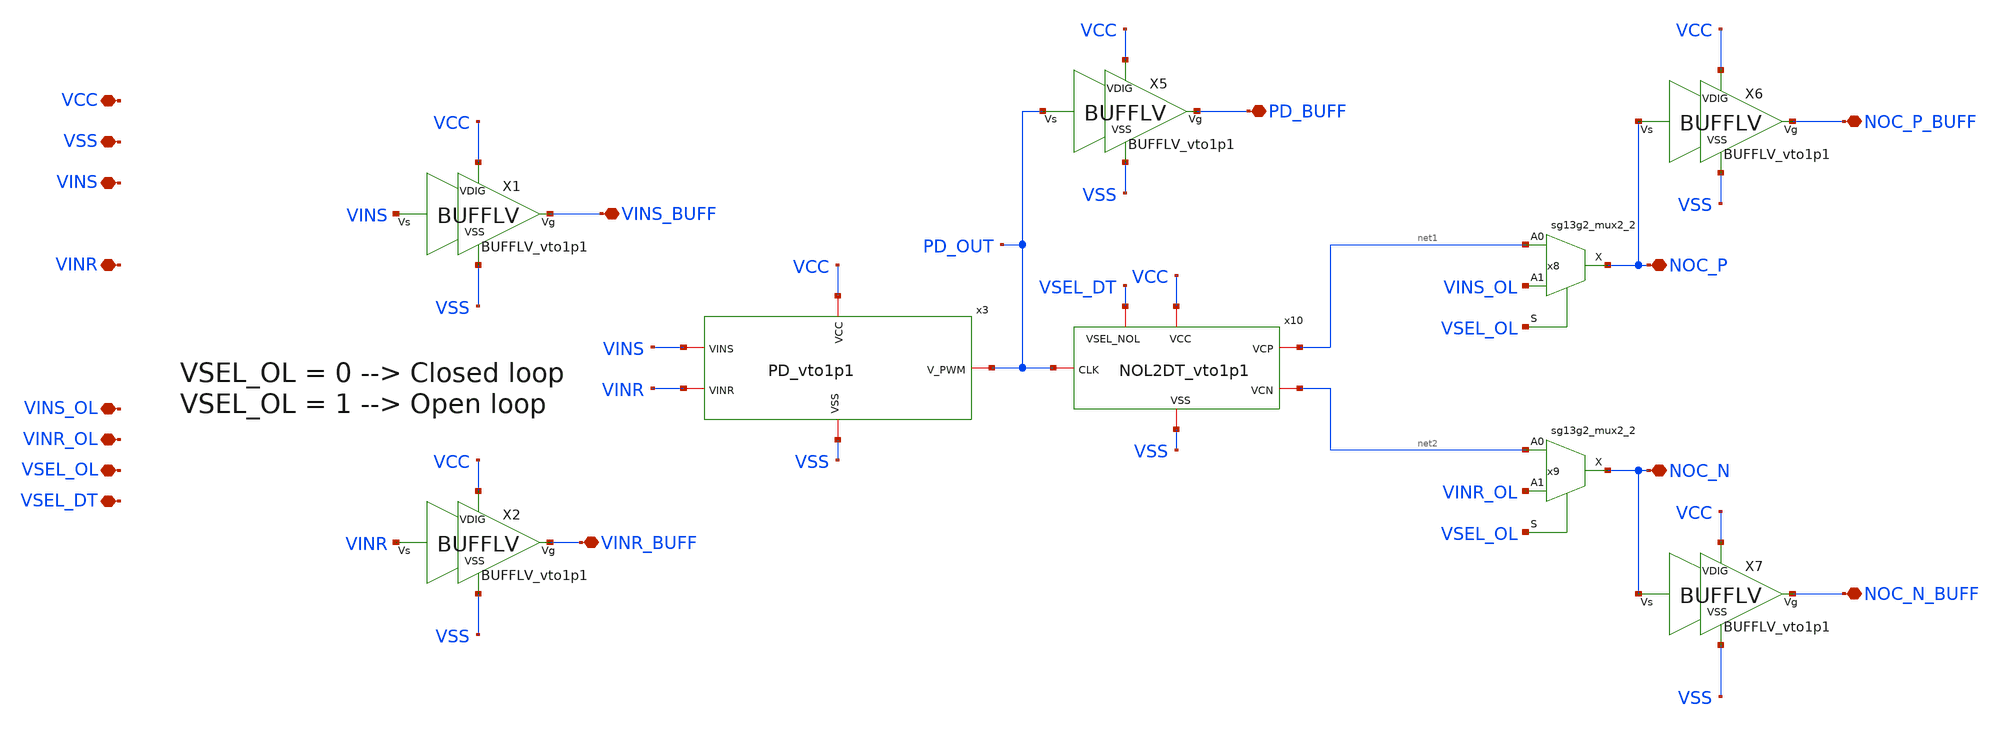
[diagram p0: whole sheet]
** sch_path: xschem/Digital_Block/DB.sch
* IHP-GmbH/IHP-Open-PDK/ihp-sg13g2/libs.tech/xschem/sg13g2_stdcells/sg13g2_buf_1.sch:
* Copyright 2023 IHP PDK Authors
* Licensed under the Apache License, Version 2.0 (the "License");
**.subckt DB VCC VSS VINS VINR NOC_P NOC_N VINS_BUFF VINR_BUFF PD_BUFF NOC_P_BUFF NOC_N_BUFF VINS_OL
*+ VINR_OL VSEL_OL VSEL_DT
*.iopin VCC
*.iopin VSS
*.iopin VINS
*.iopin VINR
*.iopin NOC_P
*.iopin NOC_N
*.iopin VINS_BUFF
*.iopin VINR_BUFF
*.iopin PD_BUFF
*.iopin NOC_P_BUFF
*.iopin NOC_N_BUFF
*.iopin VINS_OL
*.iopin VINR_OL
*.iopin VSEL_OL
*.iopin VSEL_DT
x3 VCC VSS VINS PD_OUT VINR PD_vto1p1
X1 VINS VINS_BUFF VCC VSS BUFFLV_vto1p1
X2 VINR VINR_BUFF VCC VSS BUFFLV_vto1p1
X5 PD_OUT PD_BUFF VCC VSS BUFFLV_vto1p1
X6 NOC_P NOC_P_BUFF VCC VSS BUFFLV_vto1p1
X7 NOC_N NOC_N_BUFF VCC VSS BUFFLV_vto1p1
x8 NOC_P net1 VINS_OL VSEL_OL VCC VSS sg13g2_mux2_2
x9 NOC_N net2 VINR_OL VSEL_OL VCC VSS sg13g2_mux2_2
x10 VCC VSS net1 PD_OUT net2 VSEL_DT NOL2DT_vto1p1
**.ends

* expanding   symbol:  xschem/PD/PD_vto1p1.sym # of pins=5
** sym_path: xschem/PD/PD_vto1p1.sym
** sch_path: xschem/PD/PD_vto1p1.sch
.subckt PD_vto1p1 VCC VSS VINS V_PWM VINR
*.iopin V_PWM
*.iopin VCC
*.iopin VSS
*.iopin VINS
*.iopin VINR
x3 V_N net2 V_PWM VCC VSS sg13g2_nor2_1
x1 V_PWM V_N net1 VCC VSS sg13g2_nor2_1
x4 VCC VSS VFE1 VINR net2 SPG_vto1p1
x2 VCC VSS VFE1 VINS net1 SPG_vto1p1
.ends


* expanding   symbol:  xschem/BUFFLV/BUFFLV_vto1p1.sym # of pins=4
** sym_path: xschem/BUFFLV/BUFFLV_vto1p1.sym
** sch_path: xschem/BUFFLV/BUFFLV_vto1p1.sch
.subckt BUFFLV_vto1p1 Vs Vg VDIG VSS
*.iopin VDIG
*.ipin Vs
*.opin Vg
*.iopin VSS
x7 net2 net1 VDIG VSS sg13g2_buf_4
x2 net1 Vs VDIG VSS sg13g2_buf_1
x1 net3 net2 VDIG VSS sg13g2_buf_16
x3[0] Vg net3 VDIG VSS sg13g2_buf_16
x3[1] Vg net3 VDIG VSS sg13g2_buf_16
x3[2] Vg net3 VDIG VSS sg13g2_buf_16
x3[3] Vg net3 VDIG VSS sg13g2_buf_16
.ends


* expanding   symbol:  sg13g2_stdcells/sg13g2_mux2_2.sym # of pins=4
** sym_path: sg13g2_stdcells/sg13g2_mux2_2.sym
** sch_path: sg13g2_stdcells/sg13g2_mux2_2.sch
.subckt sg13g2_mux2_2 X A0 A1 S VDD VSS
*.ipin S
*.ipin A0
*.ipin A1
*.opin X
*.iopin VDD
*.iopin VSS
XM1 Sb S VSS VSS sg13_lv_nmos w=550.00n l=130.00n ng=1 m=1 mm_ok=1
XM2 net1 A0 net5 VSS sg13_lv_nmos w=740.00n l=130.00n ng=1 m=1 mm_ok=1
XM3 net5 Sb VSS VSS sg13_lv_nmos w=740.00n l=130.00n ng=1 m=1 mm_ok=1
XM4 net1 A1 net4 VSS sg13_lv_nmos w=740.00n l=130.00n ng=1 m=1 mm_ok=1
XM5 net4 S VSS VSS sg13_lv_nmos w=740.00n l=130.00n ng=1 m=1 mm_ok=1
XM6 X net1 VSS VSS sg13_lv_nmos w=1.48u l=130.00n ng=2 m=1 mm_ok=1
XM7 Sb S VDD VDD sg13_lv_pmos w=840.00n l=130.00n ng=1 m=1 mm_ok=1
XM8 net2 S VDD VDD sg13_lv_pmos w=1.000u l=130.00n ng=1 m=1 mm_ok=1
XM9 net1 A0 net2 VDD sg13_lv_pmos w=1.000u l=130.00n ng=1 m=1 mm_ok=1
XM10 net3 Sb VDD VDD sg13_lv_pmos w=1.000u l=130.00n ng=1 m=1 mm_ok=1
XM11 net1 A1 net3 VDD sg13_lv_pmos w=1.000u l=130.00n ng=1 m=1 mm_ok=1
XM12 X net1 VDD VDD sg13_lv_pmos w=2.24u l=130.00n ng=2 m=1 mm_ok=1
.ends


* expanding   symbol:  xschem/NOL/NOL2DT_vto1p1.sym # of pins=6
** sym_path: xschem/NOL/NOL2DT_vto1p1.sym
** sch_path: xschem/NOL/NOL2DT_vto1p1.sch
.subckt NOL2DT_vto1p1 VCC VSS VCP CLK VCN VSEL_NOL
*.iopin CLK
*.iopin VCP
*.iopin VCN
*.iopin VCC
*.iopin VSS
*.iopin VSEL_NOL
x5 A1 CLK VCC VSS sg13g2_inv_1
x3 C1 A1 B1 VCC VSS sg13g2_nor2_1
x1 C2 B2 CLK VCC VSS sg13g2_nor2_1
x2 net1 B1 VCC VSS sg13g2_inv_1
x6 net2 B2 VCC VSS sg13g2_inv_2
x7 net3 net1 VCC VSS sg13g2_inv_2
x8 VCN net2 VCC VSS sg13g2_inv_4
x9 VCP net3 VCC VSS sg13g2_inv_4
x10 VCC VSS C1 net9 large_delay_vto1p1
x4 VCC VSS C2 net7 large_delay_vto1p1
x11 B2 net9 net8 VSEL_NOL VCC VSS sg13g2_mux2_2
x12 VCC VSS net4 net8 large_delay_vto1p1
x13 VCC VSS C1 net4 large_delay_vto1p1
x14 B1 net7 net6 VSEL_NOL VCC VSS sg13g2_mux2_2
x15 VCC VSS net5 net6 large_delay_vto1p1
x16 VCC VSS C2 net5 large_delay_vto1p1
.ends


* expanding   symbol:  sg13g2_stdcells/sg13g2_nor2_1.sym # of pins=3
** sym_path: sg13g2_stdcells/sg13g2_nor2_1.sym
** sch_path: sg13g2_stdcells/sg13g2_nor2_1.sch
.subckt sg13g2_nor2_1 Y A B VDD VSS
*.opin Y
*.ipin B
*.ipin A
*.iopin VDD
*.iopin VSS
XM1 Y A VSS VSS sg13_lv_nmos w=740.00n l=130.00n ng=1 m=1 mm_ok=1
XM2 Y B VSS VSS sg13_lv_nmos w=740.00n l=130.00n ng=1 m=1 mm_ok=1
XM3 net1 A VDD VDD sg13_lv_pmos w=1.12u l=130.00n ng=1 m=1 mm_ok=1
XM4 Y B net1 VDD sg13_lv_pmos w=1.12u l=130.00n ng=1 m=1 mm_ok=1
.ends


* expanding   symbol:  xschem/SPG/SPG_vto1p1.sym # of pins=5
** sym_path: xschem/SPG/SPG_vto1p1.sym
** sch_path: xschem/SPG/SPG_vto1p1.sch
.subckt SPG_vto1p1 VCC VSS VFE VIN VRE
*.iopin VIN
*.iopin VFE
*.iopin VRE
*.iopin VCC
*.iopin VSS
x1 dly8 dly7 VCC VSS sg13g2_inv_1
x2 net2 predly VCC VSS sg13g2_inv_1
x3 predly net3 VCC VSS sg13g2_inv_1
x4 net1 dly8 VCC VSS sg13g2_inv_1
x5 net3 VIN VCC VSS sg13g2_inv_2
x6 V_gatein predly VCC VSS sg13g2_inv_8
x7 VFE net2 dly8 VCC VSS sg13g2_and2_2
x8 VRE net1 predly VCC VSS sg13g2_and2_2
x9 VCC VSS V_gatein dly7 large_delay_vto1p1
.ends


* expanding   symbol:  sg13g2_stdcells/sg13g2_buf_4.sym # of pins=2
** sym_path: sg13g2_stdcells/sg13g2_buf_4.sym
** sch_path: sg13g2_stdcells/sg13g2_buf_4.sch
.subckt sg13g2_buf_4 X A VDD VSS
*.ipin A
*.opin X
*.iopin VDD
*.iopin VSS
XM1 net1 A VSS VSS sg13_lv_nmos w=740.00n l=130.00n ng=1 m=1 mm_ok=1
XM2 X net1 VSS VSS sg13_lv_nmos w=2.96u l=130.00n ng=4 m=1 mm_ok=1
XM3 net1 A VDD VDD sg13_lv_pmos w=1.68u l=130.00n ng=2 m=1 mm_ok=1
XM4 X net1 VDD VDD sg13_lv_pmos w=4.48u l=130.00n ng=4 m=1 mm_ok=1
.ends


* expanding   symbol:  sg13g2_stdcells/sg13g2_buf_1.sym # of pins=2
** sym_path: sg13g2_stdcells/sg13g2_buf_1.sym
** sch_path: sg13g2_stdcells/sg13g2_buf_1.sch
.subckt sg13g2_buf_1 X A VDD VSS
*.ipin A
*.opin X
*.iopin VDD
*.iopin VSS
XM1 net1 A VSS VSS sg13_lv_nmos w=550.00n l=130.00n ng=1 m=1 mm_ok=1
XM2 X net1 VSS VSS sg13_lv_nmos w=740.00n l=130.00n ng=1 m=1 mm_ok=1
XM3 net1 A VDD VDD sg13_lv_pmos w=840.00n l=130.00n ng=1 m=1 mm_ok=1
XM4 X net1 VDD VDD sg13_lv_pmos w=1.12u l=130.00n ng=1 m=1 mm_ok=1
.ends


* expanding   symbol:  sg13g2_stdcells/sg13g2_buf_16.sym # of pins=2
** sym_path: sg13g2_stdcells/sg13g2_buf_16.sym
** sch_path: sg13g2_stdcells/sg13g2_buf_16.sch
.subckt sg13g2_buf_16 X A VDD VSS
*.ipin A
*.opin X
*.iopin VDD
*.iopin VSS
XM1 net1 A VSS VSS sg13_lv_nmos w=4.44u l=130.00n ng=6 m=1 mm_ok=1
XM2 X net1 VSS VSS sg13_lv_nmos w=11.84u l=130.00n ng=16 m=1 mm_ok=1
XM3 net1 A VDD VDD sg13_lv_pmos w=6.72u l=130.00n ng=6 m=1 mm_ok=1
XM4 X net1 VDD VDD sg13_lv_pmos w=17.92u l=130.00n ng=16 m=1 mm_ok=1
.ends


* expanding   symbol:  sg13g2_stdcells/sg13g2_inv_1.sym # of pins=2
** sym_path: sg13g2_stdcells/sg13g2_inv_1.sym
** sch_path: sg13g2_stdcells/sg13g2_inv_1.sch
.subckt sg13g2_inv_1 Y A VDD VSS
*.opin Y
*.ipin A
*.iopin VDD
*.iopin VSS
XM1 Y A VSS VSS sg13_lv_nmos w=740.00n l=130.00n ng=1 m=1 mm_ok=1
XM2 Y A VDD VDD sg13_lv_pmos w=1.12u l=130.00n ng=1 m=1 mm_ok=1
.ends


* expanding   symbol:  sg13g2_stdcells/sg13g2_inv_2.sym # of pins=2
** sym_path: sg13g2_stdcells/sg13g2_inv_2.sym
** sch_path: sg13g2_stdcells/sg13g2_inv_2.sch
.subckt sg13g2_inv_2 Y A VDD VSS
*.opin Y
*.ipin A
*.iopin VDD
*.iopin VSS
XM1 Y A VSS VSS sg13_lv_nmos w=1.48u l=130.00n ng=2 m=1 mm_ok=1
XM2 Y A VDD VDD sg13_lv_pmos w=2.24u l=130.00n ng=2 m=1 mm_ok=1
.ends


* expanding   symbol:  sg13g2_stdcells/sg13g2_inv_4.sym # of pins=2
** sym_path: sg13g2_stdcells/sg13g2_inv_4.sym
** sch_path: sg13g2_stdcells/sg13g2_inv_4.sch
.subckt sg13g2_inv_4 Y A VDD VSS
*.ipin A
*.opin Y
*.iopin VDD
*.iopin VSS
XM1 Y A VSS VSS sg13_lv_nmos w=2.96u l=130.00n ng=4 m=1 mm_ok=1
XM2 Y A VDD VDD sg13_lv_pmos w=4.48u l=130.00n ng=4 m=1 mm_ok=1
.ends


* expanding   symbol:  xschem/large_delay/large_delay_vto1p1.sym # of pins=4
** sym_path: xschem/large_delay/large_delay_vto1p1.sym
** sch_path: xschem/large_delay/large_delay_vto1p1.sch
.subckt large_delay_vto1p1 VCC VSS VIN VOUT
*.iopin VIN
*.iopin VOUT
*.iopin VCC
*.iopin VSS
x1[0] n2 VIN VCC VSS sg13g2_dlygate4sd3_1
x1[1] n3 n2 VCC VSS sg13g2_dlygate4sd3_1
x1[2] n4 n3 VCC VSS sg13g2_dlygate4sd3_1
x1[3] n5 n4 VCC VSS sg13g2_dlygate4sd3_1
x1[4] VOUT n5 VCC VSS sg13g2_dlygate4sd3_1
.ends


* expanding   symbol:  sg13g2_stdcells/sg13g2_inv_8.sym # of pins=2
** sym_path: sg13g2_stdcells/sg13g2_inv_8.sym
** sch_path: sg13g2_stdcells/sg13g2_inv_8.sch
.subckt sg13g2_inv_8 Y A VDD VSS
*.opin Y
*.ipin A
*.iopin VDD
*.iopin VSS
XM1 Y A VSS VSS sg13_lv_nmos w=5.92u l=130.00n ng=8 m=1 mm_ok=1
XM2 Y A VDD VDD sg13_lv_pmos w=8.96u l=130.00n ng=8 m=1 mm_ok=1
.ends


* expanding   symbol:  sg13g2_stdcells/sg13g2_and2_2.sym # of pins=3
** sym_path: sg13g2_stdcells/sg13g2_and2_2.sym
** sch_path: sg13g2_stdcells/sg13g2_and2_2.sch
.subckt sg13g2_and2_2 X A B VDD VSS
*.ipin A
*.ipin B
*.opin X
*.iopin VDD
*.iopin VSS
XM1 net1 A net2 VSS sg13_lv_nmos w=640.00n l=130.00n ng=1 m=1 mm_ok=1
XM2 net2 B VSS VSS sg13_lv_nmos w=640.00n l=130.00n ng=1 m=1 mm_ok=1
XM3 X net1 VSS VSS sg13_lv_nmos w=1.48u l=130.00n ng=2 m=1 mm_ok=1
XM4 net1 B VDD VDD sg13_lv_pmos w=840.00n l=130.00n ng=1 m=1 mm_ok=1
XM5 net1 A VDD VDD sg13_lv_pmos w=840.00n l=130.00n ng=1 m=1 mm_ok=1
XM6 X net1 VDD VDD sg13_lv_pmos w=2.24u l=130.00n ng=2 m=1 mm_ok=1
.ends


* expanding   symbol:  sg13g2_stdcells/sg13g2_dlygate4sd3_1.sym # of pins=2
** sym_path: sg13g2_stdcells/sg13g2_dlygate4sd3_1.sym
** sch_path: sg13g2_stdcells/sg13g2_dlygate4sd3_1.sch
.subckt sg13g2_dlygate4sd3_1 X A VDD VSS
*.ipin A
*.opin X
*.iopin VDD
*.iopin VSS
XM1 net3 A VSS VSS sg13_lv_nmos w=420.00n l=130.00n ng=1 m=1 mm_ok=1
XM2 net1 net3 VSS VSS sg13_lv_nmos w=420.00n l=500.0n ng=1 m=1 mm_ok=1
XM3 net2 net1 VSS VSS sg13_lv_nmos w=420.00n l=500.0n ng=1 m=1 mm_ok=1
XM4 X net2 VSS VSS sg13_lv_nmos w=740.00n l=130.00n ng=1 m=1 mm_ok=1
XM5 net3 A VDD VDD sg13_lv_pmos w=420.00n l=130.00n ng=1 m=1 mm_ok=1
XM6 net1 net3 VDD VDD sg13_lv_pmos w=1.000u l=500.0n ng=1 m=1 mm_ok=1
XM7 net2 net1 VDD VDD sg13_lv_pmos w=1.000u l=500.0n ng=1 m=1 mm_ok=1
XM8 X net2 VDD VDD sg13_lv_pmos w=1.12u l=130.00n ng=1 m=1 mm_ok=1
.ends

.end
